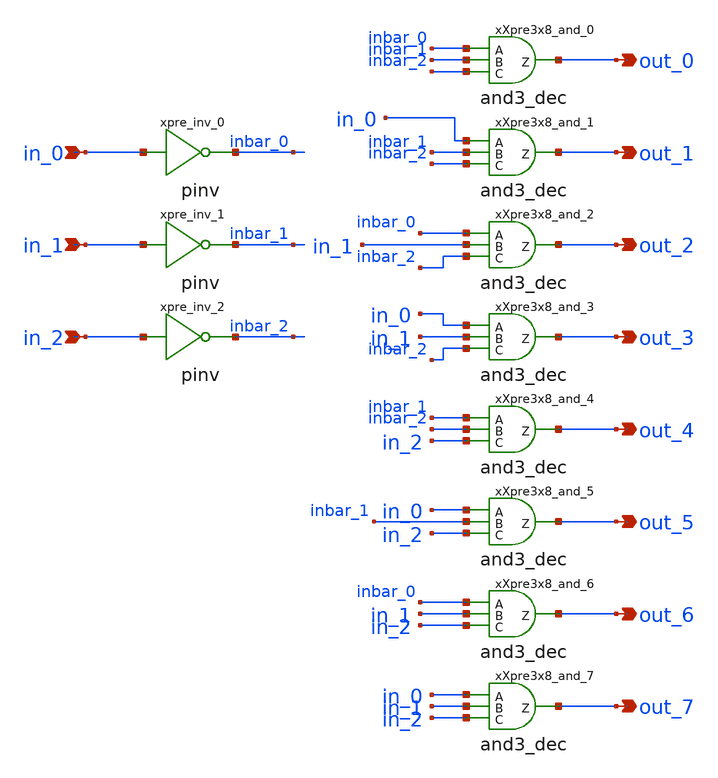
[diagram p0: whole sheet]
** sch_path: sram_4_16_scn4m/hierarchical_predecode3x8.sch
**.subckt hierarchical_predecode3x8 in_0 in_1 in_2 out_0 out_1 out_2 out_3 out_4 out_5 out_6 out_7
*.ipin in_0
*.ipin in_1
*.ipin in_2
*.opin out_0
*.opin out_1
*.opin out_2
*.opin out_3
*.opin out_4
*.opin out_5
*.opin out_6
*.opin out_7
xpre_inv_0 in_0 inbar_0 vdd gnd pinv
xpre_inv_1 in_1 inbar_1 vdd gnd pinv
xpre_inv_2 in_2 inbar_2 vdd gnd pinv
xXpre3x8_and_0 inbar_0 inbar_1 inbar_2 out_0 vdd gnd and3_dec
xXpre3x8_and_1 in_0 inbar_1 inbar_2 out_1 vdd gnd and3_dec
xXpre3x8_and_2 inbar_0 in_1 inbar_2 out_2 vdd gnd and3_dec
xXpre3x8_and_3 in_0 in_1 inbar_2 out_3 vdd gnd and3_dec
xXpre3x8_and_4 inbar_1 inbar_2 in_2 out_4 vdd gnd and3_dec
xXpre3x8_and_5 in_0 inbar_1 in_2 out_5 vdd gnd and3_dec
xXpre3x8_and_6 inbar_0 in_1 in_2 out_6 vdd gnd and3_dec
xXpre3x8_and_7 in_0 in_1 in_2 out_7 vdd gnd and3_dec
**.ends
.end
